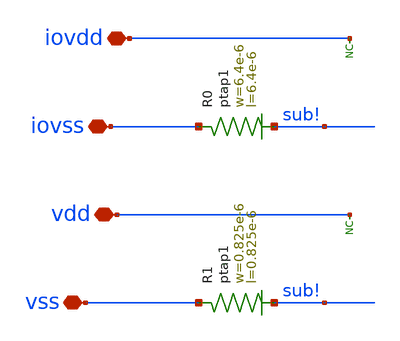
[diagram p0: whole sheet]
** sch_path: ihp-sg13g2/libs.ref/sg13g2_io/sch/xschem/sg13g2_Filler200.sch
**.subckt sg13g2_Filler200 iovdd iovss vdd vss
*.iopin iovdd
*.iopin iovss
*.iopin vdd
*.iopin vss
* noconn iovdd
* noconn vdd
XR0 iovss sub! ptap1 R=14.72 w=6.4e-6 l=6.4e-6
XR1 vss sub! ptap1 R=246.2 w=0.825e-6 l=0.825e-6
**.ends
.end
